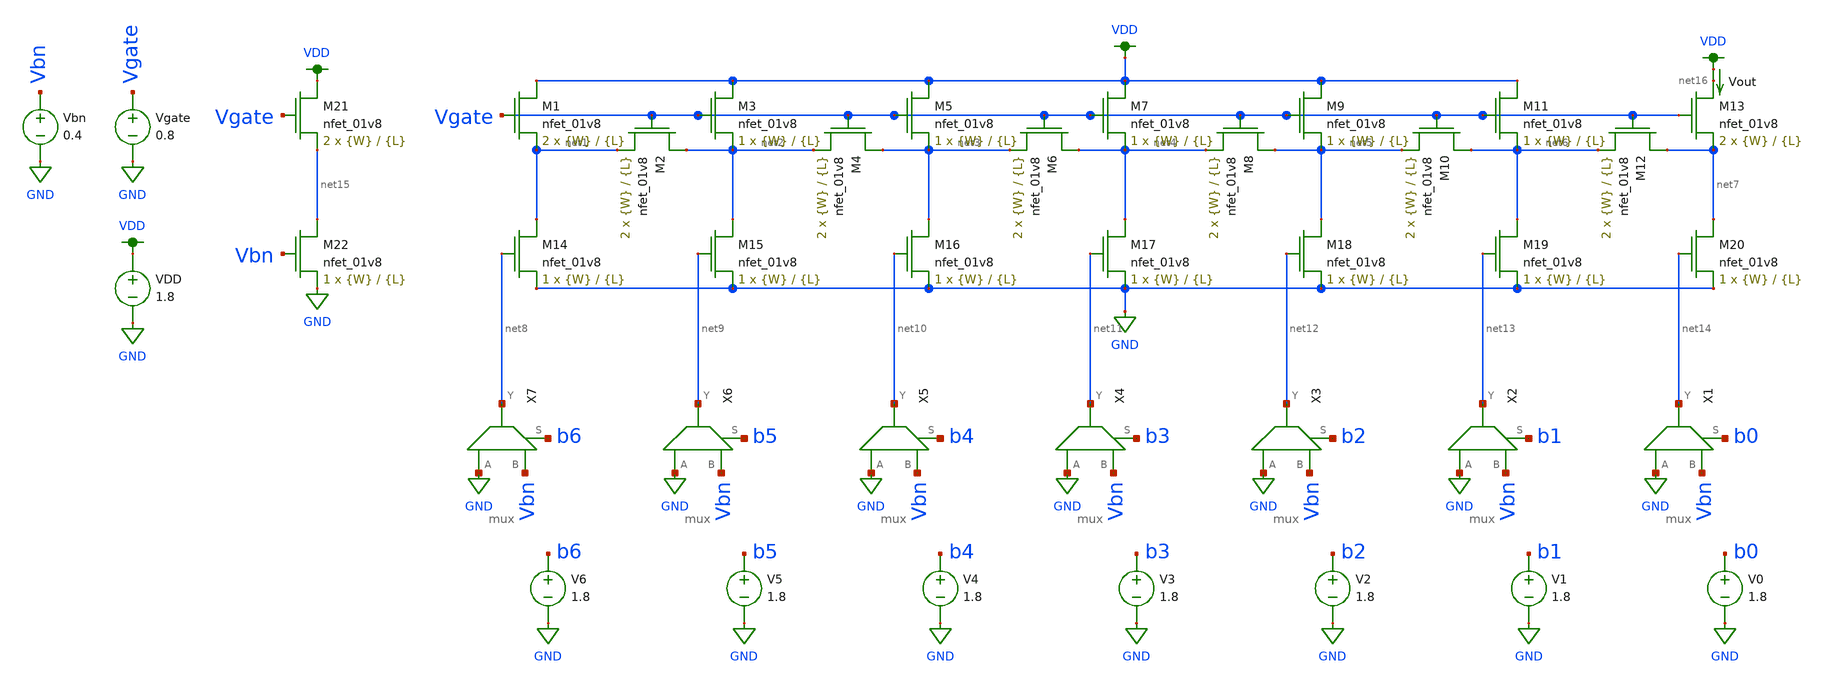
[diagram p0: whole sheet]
** sch_path: schematics/please_work_dac.sch
**.subckt please_work_dac
XM1 VDD Vgate net1 GND sky130_fd_pr__nfet_01v8 L={L} W={W} nf=1 ad='int((nf+1)/2) * W/nf * 0.29' as='int((nf+2)/2) * W/nf * 0.29'
+ pd='2*int((nf+1)/2) * (W/nf + 0.29)' ps='2*int((nf+2)/2) * (W/nf + 0.29)' nrd='0.29 / W' nrs='0.29 / W'
+ sa=0 sb=0 sd=0 mult=2 m=2
XM2 net2 Vgate net1 GND sky130_fd_pr__nfet_01v8 L={L} W={W} nf=1 ad='int((nf+1)/2) * W/nf * 0.29' as='int((nf+2)/2) * W/nf * 0.29'
+ pd='2*int((nf+1)/2) * (W/nf + 0.29)' ps='2*int((nf+2)/2) * (W/nf + 0.29)' nrd='0.29 / W' nrs='0.29 / W'
+ sa=0 sb=0 sd=0 mult=2 m=2
XM3 VDD Vgate net2 GND sky130_fd_pr__nfet_01v8 L={L} W={W} nf=1 ad='int((nf+1)/2) * W/nf * 0.29' as='int((nf+2)/2) * W/nf * 0.29'
+ pd='2*int((nf+1)/2) * (W/nf + 0.29)' ps='2*int((nf+2)/2) * (W/nf + 0.29)' nrd='0.29 / W' nrs='0.29 / W'
+ sa=0 sb=0 sd=0 mult=1 m=1
XM4 net3 Vgate net2 GND sky130_fd_pr__nfet_01v8 L={L} W={W} nf=1 ad='int((nf+1)/2) * W/nf * 0.29' as='int((nf+2)/2) * W/nf * 0.29'
+ pd='2*int((nf+1)/2) * (W/nf + 0.29)' ps='2*int((nf+2)/2) * (W/nf + 0.29)' nrd='0.29 / W' nrs='0.29 / W'
+ sa=0 sb=0 sd=0 mult=2 m=2
XM5 VDD Vgate net3 GND sky130_fd_pr__nfet_01v8 L={L} W={W} nf=1 ad='int((nf+1)/2) * W/nf * 0.29' as='int((nf+2)/2) * W/nf * 0.29'
+ pd='2*int((nf+1)/2) * (W/nf + 0.29)' ps='2*int((nf+2)/2) * (W/nf + 0.29)' nrd='0.29 / W' nrs='0.29 / W'
+ sa=0 sb=0 sd=0 mult=1 m=1
XM6 net4 Vgate net3 GND sky130_fd_pr__nfet_01v8 L={L} W={W} nf=1 ad='int((nf+1)/2) * W/nf * 0.29' as='int((nf+2)/2) * W/nf * 0.29'
+ pd='2*int((nf+1)/2) * (W/nf + 0.29)' ps='2*int((nf+2)/2) * (W/nf + 0.29)' nrd='0.29 / W' nrs='0.29 / W'
+ sa=0 sb=0 sd=0 mult=2 m=2
XM7 VDD Vgate net4 GND sky130_fd_pr__nfet_01v8 L={L} W={W} nf=1 ad='int((nf+1)/2) * W/nf * 0.29' as='int((nf+2)/2) * W/nf * 0.29'
+ pd='2*int((nf+1)/2) * (W/nf + 0.29)' ps='2*int((nf+2)/2) * (W/nf + 0.29)' nrd='0.29 / W' nrs='0.29 / W'
+ sa=0 sb=0 sd=0 mult=1 m=1
XM8 net5 Vgate net4 GND sky130_fd_pr__nfet_01v8 L={L} W={W} nf=1 ad='int((nf+1)/2) * W/nf * 0.29' as='int((nf+2)/2) * W/nf * 0.29'
+ pd='2*int((nf+1)/2) * (W/nf + 0.29)' ps='2*int((nf+2)/2) * (W/nf + 0.29)' nrd='0.29 / W' nrs='0.29 / W'
+ sa=0 sb=0 sd=0 mult=2 m=2
XM9 VDD Vgate net5 GND sky130_fd_pr__nfet_01v8 L={L} W={W} nf=1 ad='int((nf+1)/2) * W/nf * 0.29' as='int((nf+2)/2) * W/nf * 0.29'
+ pd='2*int((nf+1)/2) * (W/nf + 0.29)' ps='2*int((nf+2)/2) * (W/nf + 0.29)' nrd='0.29 / W' nrs='0.29 / W'
+ sa=0 sb=0 sd=0 mult=1 m=1
XM10 net6 Vgate net5 GND sky130_fd_pr__nfet_01v8 L={L} W={W} nf=1 ad='int((nf+1)/2) * W/nf * 0.29' as='int((nf+2)/2) * W/nf * 0.29'
+ pd='2*int((nf+1)/2) * (W/nf + 0.29)' ps='2*int((nf+2)/2) * (W/nf + 0.29)' nrd='0.29 / W' nrs='0.29 / W'
+ sa=0 sb=0 sd=0 mult=2 m=2
XM11 VDD Vgate net6 GND sky130_fd_pr__nfet_01v8 L={L} W={W} nf=1 ad='int((nf+1)/2) * W/nf * 0.29' as='int((nf+2)/2) * W/nf * 0.29'
+ pd='2*int((nf+1)/2) * (W/nf + 0.29)' ps='2*int((nf+2)/2) * (W/nf + 0.29)' nrd='0.29 / W' nrs='0.29 / W'
+ sa=0 sb=0 sd=0 mult=1 m=1
XM12 net7 Vgate net6 GND sky130_fd_pr__nfet_01v8 L={L} W={W} nf=1 ad='int((nf+1)/2) * W/nf * 0.29' as='int((nf+2)/2) * W/nf * 0.29'
+ pd='2*int((nf+1)/2) * (W/nf + 0.29)' ps='2*int((nf+2)/2) * (W/nf + 0.29)' nrd='0.29 / W' nrs='0.29 / W'
+ sa=0 sb=0 sd=0 mult=2 m=2
XM13 net16 Vgate net7 GND sky130_fd_pr__nfet_01v8 L={L} W={W} nf=1 ad='int((nf+1)/2) * W/nf * 0.29' as='int((nf+2)/2) * W/nf * 0.29'
+ pd='2*int((nf+1)/2) * (W/nf + 0.29)' ps='2*int((nf+2)/2) * (W/nf + 0.29)' nrd='0.29 / W' nrs='0.29 / W'
+ sa=0 sb=0 sd=0 mult=2 m=2
XM14 net1 net8 GND GND sky130_fd_pr__nfet_01v8 L={L} W={W} nf=1 ad='int((nf+1)/2) * W/nf * 0.29' as='int((nf+2)/2) * W/nf * 0.29'
+ pd='2*int((nf+1)/2) * (W/nf + 0.29)' ps='2*int((nf+2)/2) * (W/nf + 0.29)' nrd='0.29 / W' nrs='0.29 / W'
+ sa=0 sb=0 sd=0 mult=1 m=1
XM15 net2 net9 GND GND sky130_fd_pr__nfet_01v8 L={L} W={W} nf=1 ad='int((nf+1)/2) * W/nf * 0.29' as='int((nf+2)/2) * W/nf * 0.29'
+ pd='2*int((nf+1)/2) * (W/nf + 0.29)' ps='2*int((nf+2)/2) * (W/nf + 0.29)' nrd='0.29 / W' nrs='0.29 / W'
+ sa=0 sb=0 sd=0 mult=1 m=1
XM16 net3 net10 GND GND sky130_fd_pr__nfet_01v8 L={L} W={W} nf=1 ad='int((nf+1)/2) * W/nf * 0.29' as='int((nf+2)/2) * W/nf * 0.29'
+ pd='2*int((nf+1)/2) * (W/nf + 0.29)' ps='2*int((nf+2)/2) * (W/nf + 0.29)' nrd='0.29 / W' nrs='0.29 / W'
+ sa=0 sb=0 sd=0 mult=1 m=1
XM17 net4 net11 GND GND sky130_fd_pr__nfet_01v8 L={L} W={W} nf=1 ad='int((nf+1)/2) * W/nf * 0.29' as='int((nf+2)/2) * W/nf * 0.29'
+ pd='2*int((nf+1)/2) * (W/nf + 0.29)' ps='2*int((nf+2)/2) * (W/nf + 0.29)' nrd='0.29 / W' nrs='0.29 / W'
+ sa=0 sb=0 sd=0 mult=1 m=1
XM18 net5 net12 GND GND sky130_fd_pr__nfet_01v8 L={L} W={W} nf=1 ad='int((nf+1)/2) * W/nf * 0.29' as='int((nf+2)/2) * W/nf * 0.29'
+ pd='2*int((nf+1)/2) * (W/nf + 0.29)' ps='2*int((nf+2)/2) * (W/nf + 0.29)' nrd='0.29 / W' nrs='0.29 / W'
+ sa=0 sb=0 sd=0 mult=1 m=1
XM19 net6 net13 GND GND sky130_fd_pr__nfet_01v8 L={L} W={W} nf=1 ad='int((nf+1)/2) * W/nf * 0.29' as='int((nf+2)/2) * W/nf * 0.29'
+ pd='2*int((nf+1)/2) * (W/nf + 0.29)' ps='2*int((nf+2)/2) * (W/nf + 0.29)' nrd='0.29 / W' nrs='0.29 / W'
+ sa=0 sb=0 sd=0 mult=1 m=1
XM20 net7 net14 GND GND sky130_fd_pr__nfet_01v8 L={L} W={W} nf=1 ad='int((nf+1)/2) * W/nf * 0.29' as='int((nf+2)/2) * W/nf * 0.29'
+ pd='2*int((nf+1)/2) * (W/nf + 0.29)' ps='2*int((nf+2)/2) * (W/nf + 0.29)' nrd='0.29 / W' nrs='0.29 / W'
+ sa=0 sb=0 sd=0 mult=1 m=1
Vgate Vgate GND 0.8
XM21 VDD Vgate net15 GND sky130_fd_pr__nfet_01v8 L={L} W={W} nf=1 ad='int((nf+1)/2) * W/nf * 0.29' as='int((nf+2)/2) * W/nf * 0.29'
+ pd='2*int((nf+1)/2) * (W/nf + 0.29)' ps='2*int((nf+2)/2) * (W/nf + 0.29)' nrd='0.29 / W' nrs='0.29 / W'
+ sa=0 sb=0 sd=0 mult=2 m=2
XM22 net15 Vbn GND GND sky130_fd_pr__nfet_01v8 L={L} W={W} nf=1 ad='int((nf+1)/2) * W/nf * 0.29' as='int((nf+2)/2) * W/nf * 0.29'
+ pd='2*int((nf+1)/2) * (W/nf + 0.29)' ps='2*int((nf+2)/2) * (W/nf + 0.29)' nrd='0.29 / W' nrs='0.29 / W'
+ sa=0 sb=0 sd=0 mult=1 m=1
X1 GND Vbn net14 b0 mux
X2 GND Vbn net13 b1 mux
X3 GND Vbn net12 b2 mux
X4 GND Vbn net11 b3 mux
X5 GND Vbn net10 b4 mux
X6 GND Vbn net9 b5 mux
X7 GND Vbn net8 b6 mux
V0 b0 GND 1.8
V1 b1 GND 1.8
V2 b2 GND 1.8
V3 b3 GND 1.8
V4 b4 GND 1.8
V5 b5 GND 1.8
V6 b6 GND 1.8
Vout VDD net16 0
.save i(vout)
VDD VDD GND 1.8
Vbn Vbn GND 0.4
**** begin user architecture code

.param W=1
.param L=8
.control
set wr_vecnames
set wr_singlescale
let code = 0
  while code < 128
    if code eq 0
      let b0 = 0
    else
      let b0 = code % 2
    end
    if floor(code / 2) eq 0
      let b1 = 0
    else
      let b1 = floor(code / 2) % 2
    end
    if floor(code / 4) eq 0
      let b2 = 0
    else
      let b2 = floor(code / 4) % 2
    end
    if floor(code / 8) eq 0
      let b3 = 0
    else
      let b3 = floor(code / 8) % 2
    end
    if floor(code / 16) eq 0
      let b4 = 0
    else
      let b4 = floor(code / 16) % 2
    end
    if floor(code / 32) eq 0
      let b5 = 0
    else
      let b5 = floor(code / 32) % 2
    end
    if floor(code / 64) eq 0
      let b6 = 0
    else
      let b6 = floor(code / 64) % 2
    end
    alter vb0 $&b0
    alter vb1 $&b1
    alter vb2 $&b2
    alter vb3 $&b3
    alter vb4 $&b4
    alter vb5 $&b5
    alter vb6 $&b6
    save all
    op
    wrdata ~/Documents/current-output-dac-vlsi/simulations/dac_inf_sim.txt i(Vout)
    if code eq 0
      set appendwrite
      set wr_vecnames = FALSE
    end
    let code = code + 1
  end
  quit
.endc


.option wnflag=1
.param MC_SWITCH=0.0
.lib ~/skywater/skywater-pdk/libraries/sky130_fd_pr_ngspice/latest/models/sky130.lib.spice tt

**** end user architecture code
**.ends

* expanding   symbol:  /home/madvlsi/Documents/current-output-dac-vlsi/schematics/mux.sym # of
*+ pins=4
** sym_path: /home/madvlsi/Documents/current-output-dac-vlsi/schematics/mux.sym
** sch_path: /home/madvlsi/Documents/current-output-dac-vlsi/schematics/mux.sch
.subckt mux A B Y S
*.ipin S
*.ipin A
*.opin Y
*.ipin B
XM1 net1 S GND GND sky130_fd_pr__nfet_01v8 L=0.15 W=1 nf=1 ad='int((nf+1)/2) * W/nf * 0.29' as='int((nf+2)/2) * W/nf * 0.29'
+ pd='2*int((nf+1)/2) * (W/nf + 0.29)' ps='2*int((nf+2)/2) * (W/nf + 0.29)' nrd='0.29 / W' nrs='0.29 / W'
+ sa=0 sb=0 sd=0 mult=1 m=1
XM2 net1 S VDD VDD sky130_fd_pr__pfet_01v8 L=0.15 W=1 nf=1 ad='int((nf+1)/2) * W/nf * 0.29' as='int((nf+2)/2) * W/nf * 0.29'
+ pd='2*int((nf+1)/2) * (W/nf + 0.29)' ps='2*int((nf+2)/2) * (W/nf + 0.29)' nrd='0.29 / W' nrs='0.29 / W'
+ sa=0 sb=0 sd=0 mult=1 m=1
XM3 Y S B GND sky130_fd_pr__nfet_01v8 L=0.15 W=1 nf=1 ad='int((nf+1)/2) * W/nf * 0.29' as='int((nf+2)/2) * W/nf * 0.29'
+ pd='2*int((nf+1)/2) * (W/nf + 0.29)' ps='2*int((nf+2)/2) * (W/nf + 0.29)' nrd='0.29 / W' nrs='0.29 / W'
+ sa=0 sb=0 sd=0 mult=1 m=1
XM4 A net1 Y GND sky130_fd_pr__nfet_01v8 L=0.15 W=1 nf=1 ad='int((nf+1)/2) * W/nf * 0.29' as='int((nf+2)/2) * W/nf * 0.29'
+ pd='2*int((nf+1)/2) * (W/nf + 0.29)' ps='2*int((nf+2)/2) * (W/nf + 0.29)' nrd='0.29 / W' nrs='0.29 / W'
+ sa=0 sb=0 sd=0 mult=1 m=1
.ends

.GLOBAL GND
.GLOBAL VDD
.end
